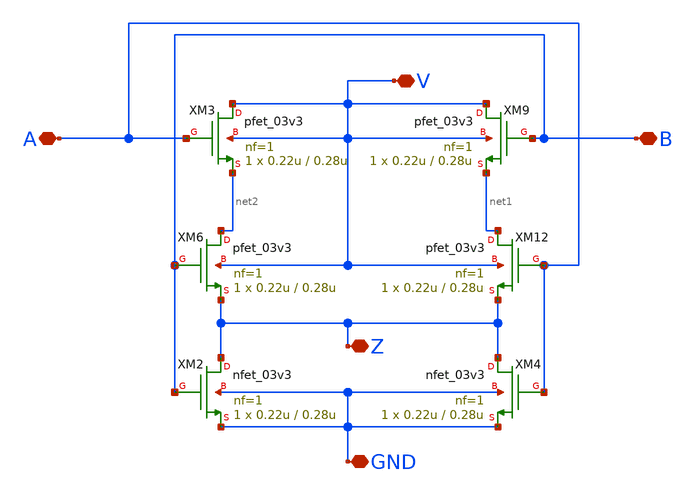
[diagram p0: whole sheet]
** sch_path: SAR_ADC/xschem/designs/norgate.sch
**.subckt norgate GND A B V Z
*.iopin GND
*.iopin A
*.iopin B
*.iopin V
*.iopin Z
XM3 V A net2 V pfet_03v3 L=0.28u W=0.22u nf=1 ad='int((nf+1)/2) * W/nf * 0.18u' as='int((nf+2)/2) * W/nf * 0.18u'
+ pd='2*int((nf+1)/2) * (W/nf + 0.18u)' ps='2*int((nf+2)/2) * (W/nf + 0.18u)' nrd='0.18u / W' nrs='0.18u / W'
+ sa=0 sb=0 sd=0 m=1
XM6 net2 B Z V pfet_03v3 L=0.28u W=0.22u nf=1 ad='int((nf+1)/2) * W/nf * 0.18u' as='int((nf+2)/2) * W/nf * 0.18u'
+ pd='2*int((nf+1)/2) * (W/nf + 0.18u)' ps='2*int((nf+2)/2) * (W/nf + 0.18u)' nrd='0.18u / W' nrs='0.18u / W'
+ sa=0 sb=0 sd=0 m=1
XM9 V B net1 V pfet_03v3 L=0.28u W=0.22u nf=1 ad='int((nf+1)/2) * W/nf * 0.18u' as='int((nf+2)/2) * W/nf * 0.18u'
+ pd='2*int((nf+1)/2) * (W/nf + 0.18u)' ps='2*int((nf+2)/2) * (W/nf + 0.18u)' nrd='0.18u / W' nrs='0.18u / W'
+ sa=0 sb=0 sd=0 m=1
XM12 net1 A Z V pfet_03v3 L=0.28u W=0.22u nf=1 ad='int((nf+1)/2) * W/nf * 0.18u' as='int((nf+2)/2) * W/nf * 0.18u'
+ pd='2*int((nf+1)/2) * (W/nf + 0.18u)' ps='2*int((nf+2)/2) * (W/nf + 0.18u)' nrd='0.18u / W' nrs='0.18u / W'
+ sa=0 sb=0 sd=0 m=1
XM2 Z B GND GND nfet_03v3 L=0.28u W=0.22u nf=1 ad='int((nf+1)/2) * W/nf * 0.18u' as='int((nf+2)/2) * W/nf * 0.18u'
+ pd='2*int((nf+1)/2) * (W/nf + 0.18u)' ps='2*int((nf+2)/2) * (W/nf + 0.18u)' nrd='0.18u / W' nrs='0.18u / W'
+ sa=0 sb=0 sd=0 m=1
XM4 Z A GND GND nfet_03v3 L=0.28u W=0.22u nf=1 ad='int((nf+1)/2) * W/nf * 0.18u' as='int((nf+2)/2) * W/nf * 0.18u'
+ pd='2*int((nf+1)/2) * (W/nf + 0.18u)' ps='2*int((nf+2)/2) * (W/nf + 0.18u)' nrd='0.18u / W' nrs='0.18u / W'
+ sa=0 sb=0 sd=0 m=1
**.ends
.end
